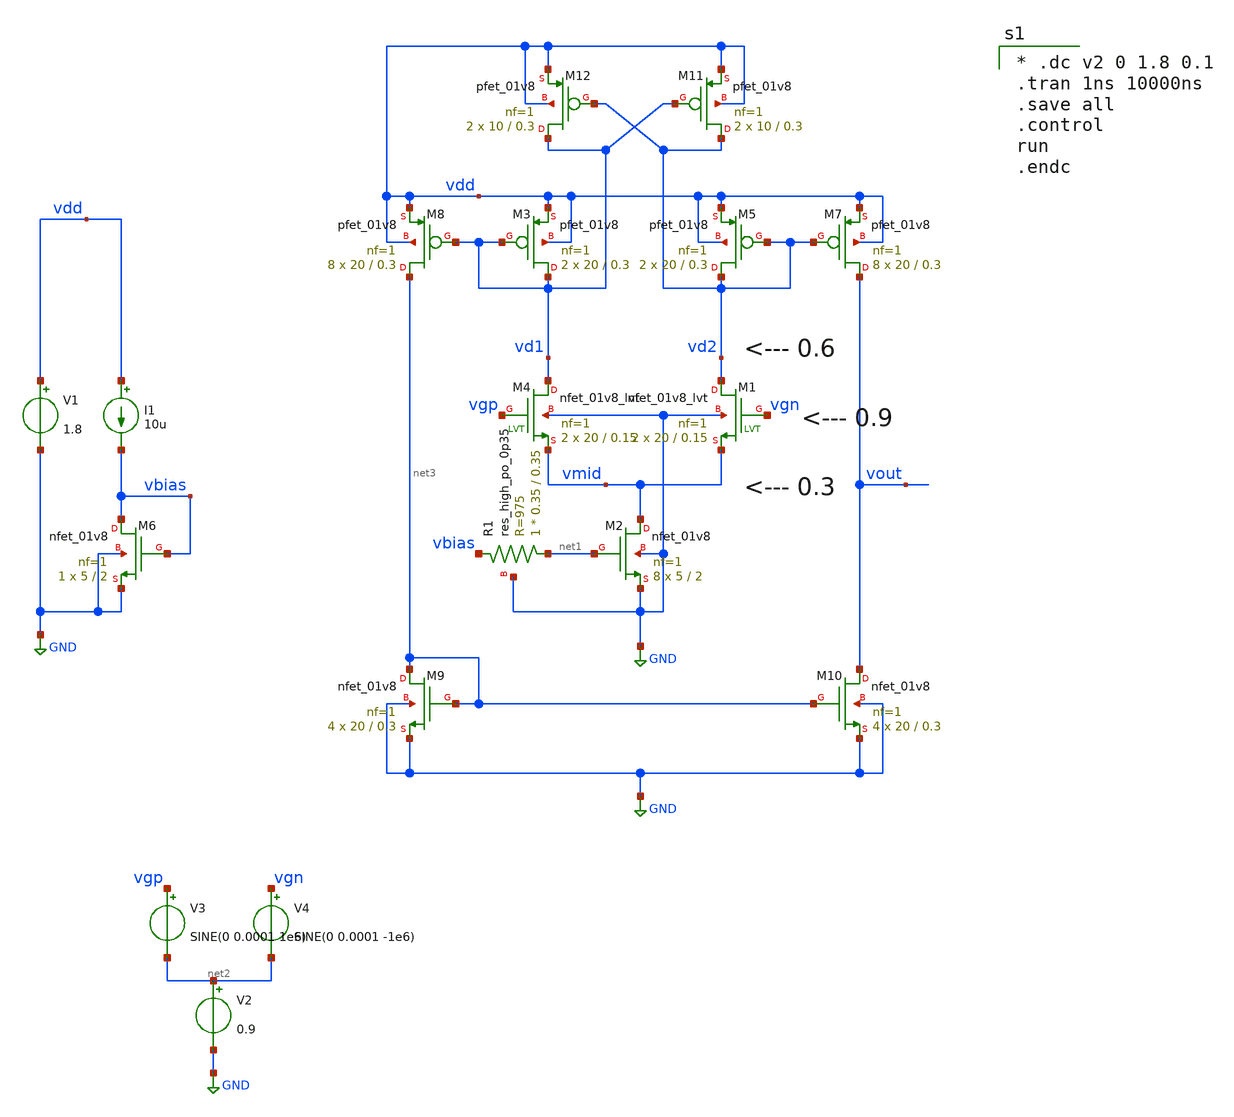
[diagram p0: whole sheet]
** sch_path: xschem/i_type_ota_tran_tb.sch
**.subckt i_type_ota_tran_tb
XM2 vmid net1 GND GND sky130_fd_pr__nfet_01v8 L=2 W=5 nf=1 ad='int((nf+1)/2) * W/nf * 0.29' as='int((nf+2)/2) * W/nf * 0.29'
+ pd='2*int((nf+1)/2) * (W/nf + 0.29)' ps='2*int((nf+2)/2) * (W/nf + 0.29)' nrd='0.29 / W' nrs='0.29 / W'
+ sa=0 sb=0 sd=0 mult=8 m=8
XM6 vbias vbias GND GND sky130_fd_pr__nfet_01v8 L=2 W=5 nf=1 ad='int((nf+1)/2) * W/nf * 0.29' as='int((nf+2)/2) * W/nf * 0.29'
+ pd='2*int((nf+1)/2) * (W/nf + 0.29)' ps='2*int((nf+2)/2) * (W/nf + 0.29)' nrd='0.29 / W' nrs='0.29 / W'
+ sa=0 sb=0 sd=0 mult=1 m=1
I1 vdd vbias 10u
XR1 net1 vbias GND sky130_fd_pr__res_high_po_0p35 L=0.35 mult=1 m=1
V1 vdd GND 1.8
V2 net2 GND 0.9
V3 vgp net2 SINE(0 0.0001 1e6)
XM4 vd1 vgp vmid GND sky130_fd_pr__nfet_01v8_lvt L=0.15 W=20 nf=1 ad='int((nf+1)/2) * W/nf * 0.29' as='int((nf+2)/2) * W/nf * 0.29'
+ pd='2*int((nf+1)/2) * (W/nf + 0.29)' ps='2*int((nf+2)/2) * (W/nf + 0.29)' nrd='0.29 / W' nrs='0.29 / W'
+ sa=0 sb=0 sd=0 mult=2 m=2
XM1 vd2 vgn vmid GND sky130_fd_pr__nfet_01v8_lvt L=0.15 W=20 nf=1 ad='int((nf+1)/2) * W/nf * 0.29' as='int((nf+2)/2) * W/nf * 0.29'
+ pd='2*int((nf+1)/2) * (W/nf + 0.29)' ps='2*int((nf+2)/2) * (W/nf + 0.29)' nrd='0.29 / W' nrs='0.29 / W'
+ sa=0 sb=0 sd=0 mult=2 m=2
XM3 vd1 vd1 vdd vdd sky130_fd_pr__pfet_01v8 L=0.3 W=20 nf=1 ad='int((nf+1)/2) * W/nf * 0.29' as='int((nf+2)/2) * W/nf * 0.29'
+ pd='2*int((nf+1)/2) * (W/nf + 0.29)' ps='2*int((nf+2)/2) * (W/nf + 0.29)' nrd='0.29 / W' nrs='0.29 / W'
+ sa=0 sb=0 sd=0 mult=2 m=2
XM5 vd2 vd2 vdd vdd sky130_fd_pr__pfet_01v8 L=0.3 W=20 nf=1 ad='int((nf+1)/2) * W/nf * 0.29' as='int((nf+2)/2) * W/nf * 0.29'
+ pd='2*int((nf+1)/2) * (W/nf + 0.29)' ps='2*int((nf+2)/2) * (W/nf + 0.29)' nrd='0.29 / W' nrs='0.29 / W'
+ sa=0 sb=0 sd=0 mult=2 m=2
XM7 vout vd2 vdd vdd sky130_fd_pr__pfet_01v8 L=0.3 W=20 nf=1 ad='int((nf+1)/2) * W/nf * 0.29' as='int((nf+2)/2) * W/nf * 0.29'
+ pd='2*int((nf+1)/2) * (W/nf + 0.29)' ps='2*int((nf+2)/2) * (W/nf + 0.29)' nrd='0.29 / W' nrs='0.29 / W'
+ sa=0 sb=0 sd=0 mult=8 m=8
XM8 net3 vd1 vdd vdd sky130_fd_pr__pfet_01v8 L=0.3 W=20 nf=1 ad='int((nf+1)/2) * W/nf * 0.29' as='int((nf+2)/2) * W/nf * 0.29'
+ pd='2*int((nf+1)/2) * (W/nf + 0.29)' ps='2*int((nf+2)/2) * (W/nf + 0.29)' nrd='0.29 / W' nrs='0.29 / W'
+ sa=0 sb=0 sd=0 mult=8 m=8
XM9 net3 net3 GND GND sky130_fd_pr__nfet_01v8 L=0.3 W=20 nf=1 ad='int((nf+1)/2) * W/nf * 0.29' as='int((nf+2)/2) * W/nf * 0.29'
+ pd='2*int((nf+1)/2) * (W/nf + 0.29)' ps='2*int((nf+2)/2) * (W/nf + 0.29)' nrd='0.29 / W' nrs='0.29 / W'
+ sa=0 sb=0 sd=0 mult=4 m=4
XM10 vout net3 GND GND sky130_fd_pr__nfet_01v8 L=0.3 W=20 nf=1 ad='int((nf+1)/2) * W/nf * 0.29' as='int((nf+2)/2) * W/nf * 0.29'
+ pd='2*int((nf+1)/2) * (W/nf + 0.29)' ps='2*int((nf+2)/2) * (W/nf + 0.29)' nrd='0.29 / W' nrs='0.29 / W'
+ sa=0 sb=0 sd=0 mult=4 m=4
XM11 vd2 vd1 vdd vdd sky130_fd_pr__pfet_01v8 L=0.3 W=10 nf=1 ad='int((nf+1)/2) * W/nf * 0.29' as='int((nf+2)/2) * W/nf * 0.29'
+ pd='2*int((nf+1)/2) * (W/nf + 0.29)' ps='2*int((nf+2)/2) * (W/nf + 0.29)' nrd='0.29 / W' nrs='0.29 / W'
+ sa=0 sb=0 sd=0 mult=2 m=2
XM12 vd1 vd2 vdd vdd sky130_fd_pr__pfet_01v8 L=0.3 W=10 nf=1 ad='int((nf+1)/2) * W/nf * 0.29' as='int((nf+2)/2) * W/nf * 0.29'
+ pd='2*int((nf+1)/2) * (W/nf + 0.29)' ps='2*int((nf+2)/2) * (W/nf + 0.29)' nrd='0.29 / W' nrs='0.29 / W'
+ sa=0 sb=0 sd=0 mult=2 m=2
V4 vgn net2 SINE(0 0.0001 -1e6)
**** begin user architecture code
.lib $::SKYWATER_MODELS/sky130.lib.spice tt
.include $::PDKPATH/libs.ref/sky130_fd_sc_hs/spice/sky130_fd_sc_hs.spice


* .dc v2 0 1.8 0.1
.tran 1ns 10000ns
.save all
.control
run
.endc


**** end user architecture code
**.ends
.GLOBAL GND
.end
